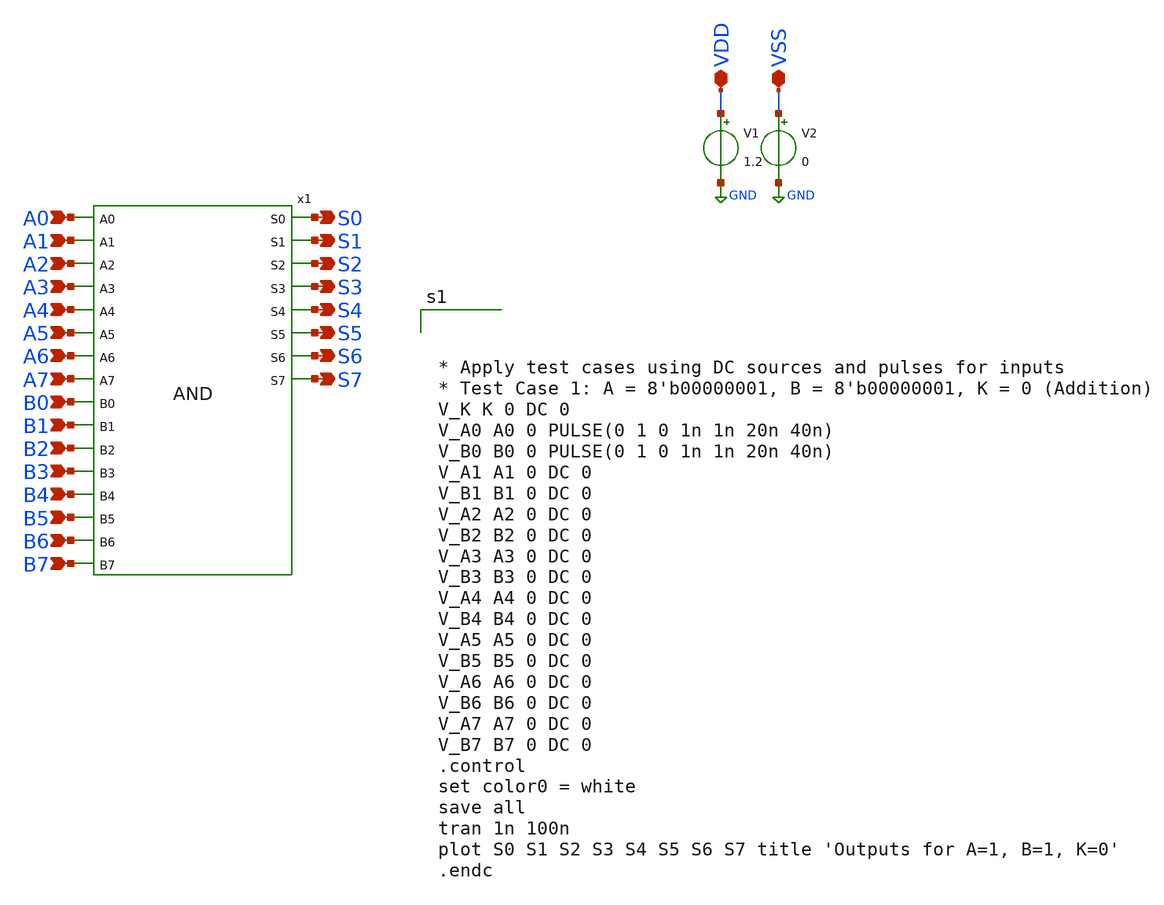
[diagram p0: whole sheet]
** sch_path: design/xschem/untitled.sch
**.subckt untitled VDD VSS A0 A1 B1 A2 B2 A3 B3 A4 B4 A5 B5 A6 B6 A7 B7 B0 S6 S7 S3 S4 S5 S0 S1 S2
*.iopin VDD
*.iopin VSS
*.ipin A0
*.ipin A1
*.ipin B1
*.ipin A2
*.ipin B2
*.ipin A3
*.ipin B3
*.ipin A4
*.ipin B4
*.ipin A5
*.ipin B5
*.ipin A6
*.ipin B6
*.ipin A7
*.ipin B7
*.ipin B0
*.opin S6
*.opin S7
*.opin S3
*.opin S4
*.opin S5
*.opin S0
*.opin S1
*.opin S2
V1 VDD GND 1.2
V2 VSS GND 0
x1 S0 A0 S1 A1 A2 S2 A3 S3 A4 S4 A5 S5 S6 A6 A7 S7 B0 B1 B2 B3 B4 B5 B6 B7 VSS VDD AND
**** begin user architecture code



* Apply test cases using DC sources and pulses for inputs
* Test Case 1: A = 8'b00000001, B = 8'b00000001, K = 0 (Addition)
V_K K 0 DC 0
V_A0 A0 0 PULSE(0 1 0 1n 1n 20n 40n)
V_B0 B0 0 PULSE(0 1 0 1n 1n 20n 40n)
V_A1 A1 0 DC 0
V_B1 B1 0 DC 0
V_A2 A2 0 DC 0
V_B2 B2 0 DC 0
V_A3 A3 0 DC 0
V_B3 B3 0 DC 0
V_A4 A4 0 DC 0
V_B4 B4 0 DC 0
V_A5 A5 0 DC 0
V_B5 B5 0 DC 0
V_A6 A6 0 DC 0
V_B6 B6 0 DC 0
V_A7 A7 0 DC 0
V_B7 B7 0 DC 0
.control
set color0 = white
save all
tran 1n 100n
plot S0 S1 S2 S3 S4 S5 S6 S7 title 'Outputs for A=1, B=1, K=0'
.endc



** opencircuitdesign pdks install
.lib $::SKYWATER_MODELS/sky130.lib.spice tt_mm


**** end user architecture code
**.ends

* expanding   symbol:  AND8/AND.sym # of pins=24
** sym_path: design/xschem/AND8/AND.sym
** sch_path: design/xschem/AND8/AND.sch
.subckt AND S0 A0 S1 A1 A2 S2 A3 S3 A4 S4 A5 S5 S6 A6 A7 S7 B0 B1 B2 B3 B4 B5 B6 B7 VSS VDD
*.opin S6
*.opin S7
*.opin S3
*.opin S4
*.opin S5
*.opin S0
*.opin S1
*.opin S2
*.ipin A0
*.ipin A1
*.ipin B1
*.ipin A2
*.ipin B2
*.ipin A3
*.ipin B3
*.ipin A4
*.ipin B4
*.ipin A5
*.ipin B5
*.ipin A6
*.ipin B6
*.ipin A7
*.ipin B7
*.ipin B0
x1 A0 A1 A2 A3 A4 A5 A6 A7 B0 B1 B2 B3 B4 B5 B6 B7 net1 net2 net3 net4 net5 net6 net7 net8
+ nand_8_bitwise
x2 net1 net2 net3 net4 net5 net6 net7 net8 S0 S1 S2 S3 S4 S5 S6 S7 not8
.ends


* expanding   symbol:  NAND/nand_8_bitwise.sym # of pins=24
** sym_path: design/xschem/NAND/nand_8_bitwise.sym
** sch_path: design/xschem/NAND/nand_8_bitwise.sch
.subckt nand_8_bitwise A0 A1 A2 A3 A4 A5 A6 A7 B0 B1 B2 B3 B4 B5 B6 B7 P0 P1 P2 P3 P4 P5 P6 P7
*.ipin B7
*.ipin B5
*.ipin B6
*.ipin B4
*.ipin B3
*.ipin B2
*.ipin B1
*.ipin B0
*.opin P7
*.opin P6
*.opin P5
*.opin P4
*.opin P3
*.opin P2
*.opin P1
*.opin P0
*.ipin A7
*.ipin A5
*.ipin A6
*.ipin A4
*.ipin A3
*.ipin A2
*.ipin A1
*.ipin A0
x1 B7 A7 VSS VDD P7 nand2
x2 B6 A6 VSS VDD P6 nand2
x3 B5 A5 VSS VDD P5 nand2
x4 B4 A4 VSS VDD P4 nand2
x5 B3 A3 VSS VDD P3 nand2
x6 B2 A2 VSS VDD P2 nand2
x7 B1 A1 VSS VDD P1 nand2
x8 B0 A0 VSS VDD P0 nand2
.ends


* expanding   symbol:  NOT/not8.sym # of pins=16
** sym_path: design/xschem/NOT/not8.sym
** sch_path: design/xschem/NOT/not8.sch
.subckt not8 A0 A1 A2 A3 A4 A5 A6 A7 S0 S1 S2 S3 S4 S5 S6 S7
*.ipin A7
*.ipin A5
*.ipin A6
*.ipin A4
*.ipin A3
*.ipin A2
*.ipin A1
*.ipin A0
*.opin S7
*.opin S6
*.opin S5
*.opin S4
*.opin S3
*.opin S2
*.opin S1
*.opin S0
x1 A3 VSS VDD S3 inv
x2 A2 VSS VDD S2 inv
x3 A1 VSS VDD S1 inv
x4 A4 VSS VDD S4 inv
x5 A5 VSS VDD S5 inv
x6 A6 VSS VDD S6 inv
x7 A0 VSS VDD S0 inv
x9 A7 VSS VDD S7 inv
.ends


* expanding   symbol:  NAND/nand2.sym # of pins=3
** sym_path: design/xschem/NAND/nand2.sym
** sch_path: design/xschem/NAND/nand2.sch
.subckt nand2 A B VSS VDD Y
*.ipin A
*.opin Y
*.ipin B
XM1 Y A VDD VDD sky130_fd_pr__pfet_01v8 L=0.15 W=3.2 nf=1 ad='int((nf+1)/2) * W/nf * 0.29' as='int((nf+2)/2) * W/nf * 0.29'
+ pd='2*int((nf+1)/2) * (W/nf + 0.29)' ps='2*int((nf+2)/2) * (W/nf + 0.29)' nrd='0.29 / W' nrs='0.29 / W'
+ sa=0 sb=0 sd=0 mult=1 m=1
XM2 Y A net1 net1 sky130_fd_pr__nfet_01v8 L=0.15 W=2 nf=1 ad='int((nf+1)/2) * W/nf * 0.29' as='int((nf+2)/2) * W/nf * 0.29'
+ pd='2*int((nf+1)/2) * (W/nf + 0.29)' ps='2*int((nf+2)/2) * (W/nf + 0.29)' nrd='0.29 / W' nrs='0.29 / W'
+ sa=0 sb=0 sd=0 mult=1 m=1
XM3 net1 B VSS VSS sky130_fd_pr__nfet_01v8 L=0.15 W=2 nf=1 ad='int((nf+1)/2) * W/nf * 0.29' as='int((nf+2)/2) * W/nf * 0.29'
+ pd='2*int((nf+1)/2) * (W/nf + 0.29)' ps='2*int((nf+2)/2) * (W/nf + 0.29)' nrd='0.29 / W' nrs='0.29 / W'
+ sa=0 sb=0 sd=0 mult=1 m=1
XM4 Y B VDD VDD sky130_fd_pr__pfet_01v8 L=0.15 W=3.2 nf=1 ad='int((nf+1)/2) * W/nf * 0.29' as='int((nf+2)/2) * W/nf * 0.29'
+ pd='2*int((nf+1)/2) * (W/nf + 0.29)' ps='2*int((nf+2)/2) * (W/nf + 0.29)' nrd='0.29 / W' nrs='0.29 / W'
+ sa=0 sb=0 sd=0 mult=1 m=1
.ends


* expanding   symbol:  INV/inv.sym # of pins=2
** sym_path: design/xschem/INV/inv.sym
** sch_path: design/xschem/INV/inv.sch
.subckt inv A VSS VDD Y
*.ipin A
*.opin Y
XM2 Y A VSS GND sky130_fd_pr__nfet_01v8 L=0.15 W=1 nf=1 ad='int((nf+1)/2) * W/nf * 0.29' as='int((nf+2)/2) * W/nf * 0.29'
+ pd='2*int((nf+1)/2) * (W/nf + 0.29)' ps='2*int((nf+2)/2) * (W/nf + 0.29)' nrd='0.29 / W' nrs='0.29 / W'
+ sa=0 sb=0 sd=0 mult=1 m=1
XM1 Y A VDD VDD sky130_fd_pr__pfet_01v8 L=0.15 W=3.21 nf=1 ad='int((nf+1)/2) * W/nf * 0.29' as='int((nf+2)/2) * W/nf * 0.29'
+ pd='2*int((nf+1)/2) * (W/nf + 0.29)' ps='2*int((nf+2)/2) * (W/nf + 0.29)' nrd='0.29 / W' nrs='0.29 / W'
+ sa=0 sb=0 sd=0 mult=1 m=1
.ends

.GLOBAL GND
.end
